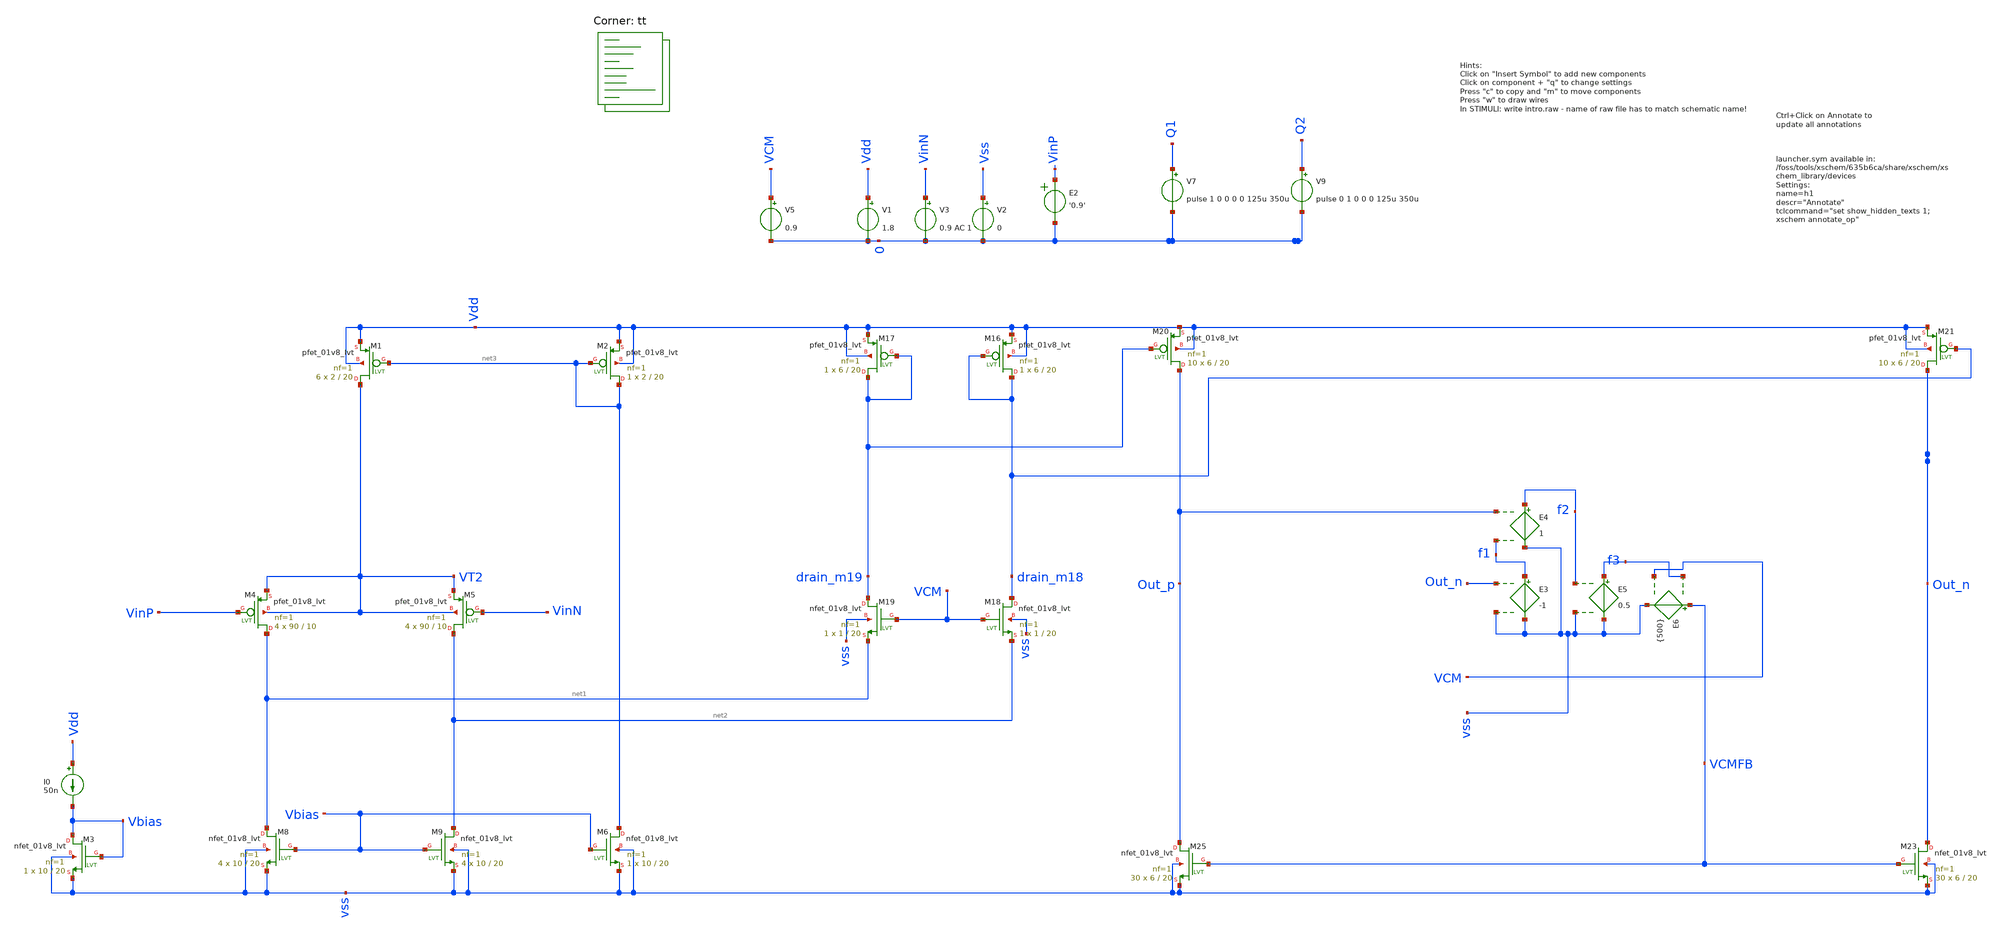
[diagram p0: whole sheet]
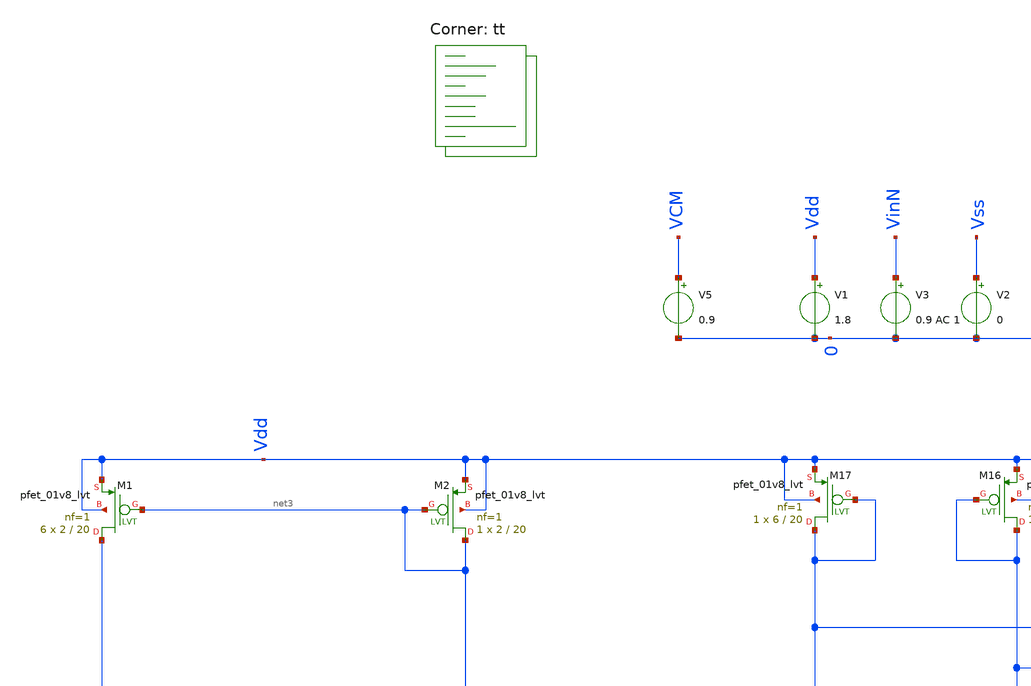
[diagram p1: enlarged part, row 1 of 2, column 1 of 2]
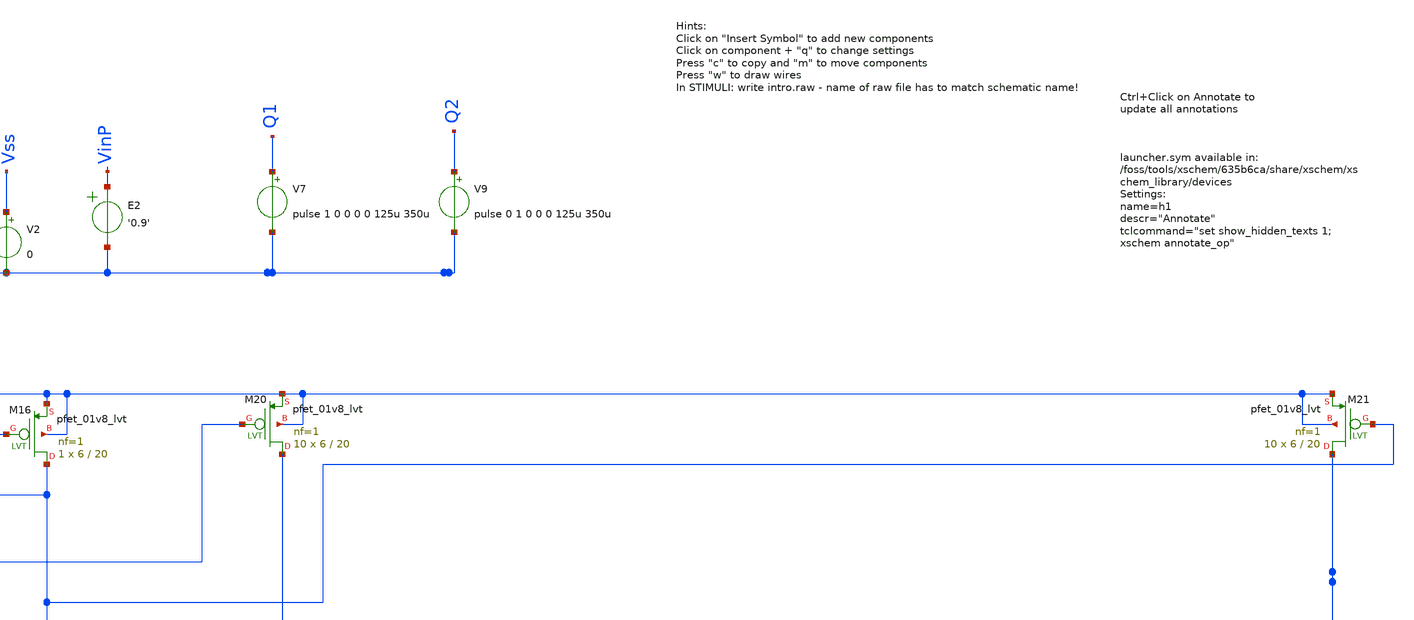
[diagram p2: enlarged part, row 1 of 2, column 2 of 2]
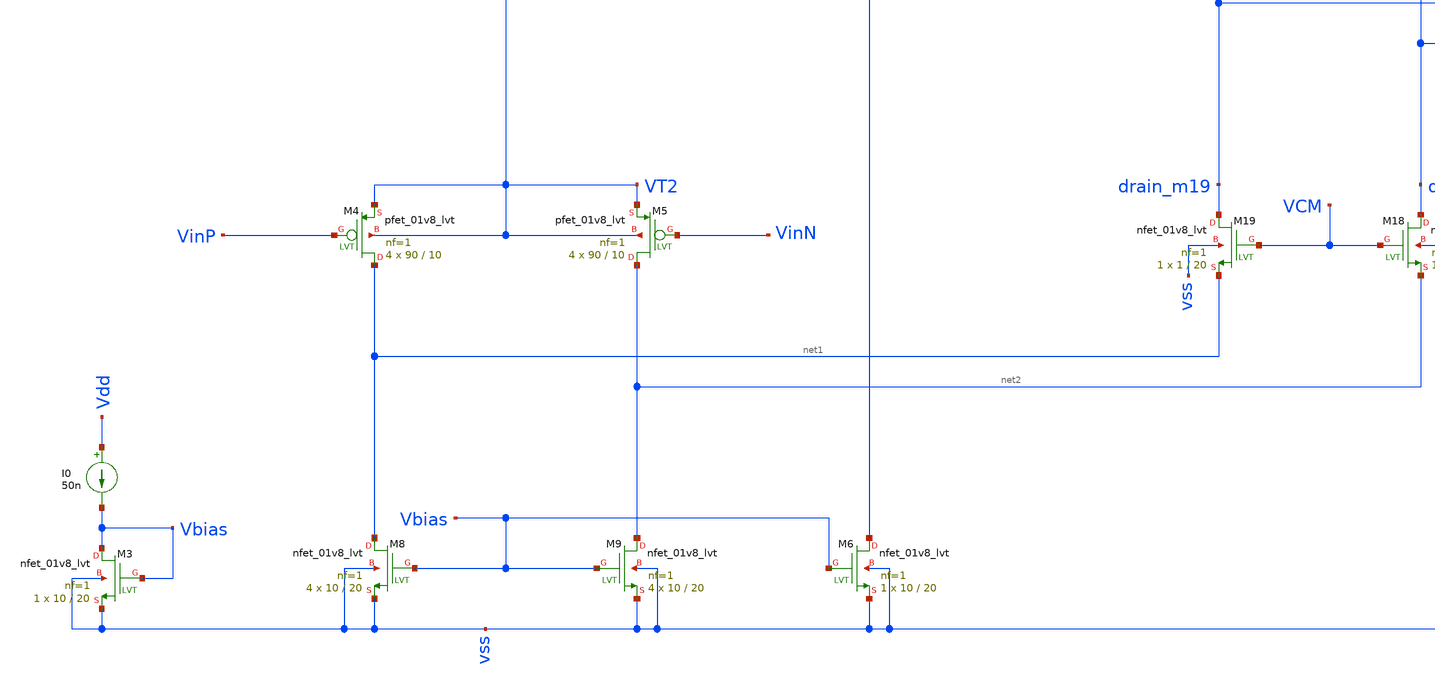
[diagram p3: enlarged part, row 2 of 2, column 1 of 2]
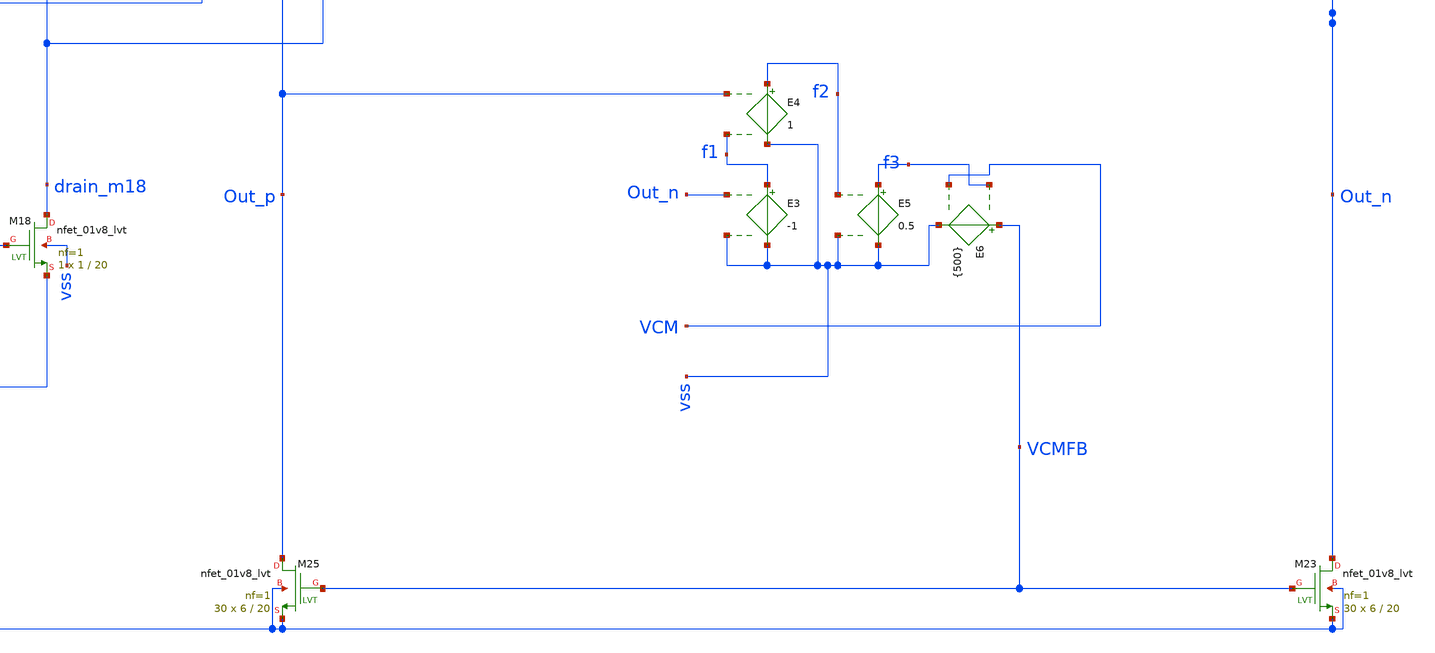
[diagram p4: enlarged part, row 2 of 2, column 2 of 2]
** sch_path: introlvt.sch
**.subckt introlvt
XM4 net1 VinP VT2 VT2 sky130_fd_pr__pfet_01v8_lvt L=10 W=90 nf=1 ad='int((nf+1)/2) * W/nf * 0.29' as='int((nf+2)/2) * W/nf * 0.29'
+ pd='2*int((nf+1)/2) * (W/nf + 0.29)' ps='2*int((nf+2)/2) * (W/nf + 0.29)' nrd='0.29 / W' nrs='0.29 / W'
+ sa=0 sb=0 sd=0 mult=4 m=4
XM5 net2 VinN VT2 VT2 sky130_fd_pr__pfet_01v8_lvt L=10 W=90 nf=1 ad='int((nf+1)/2) * W/nf * 0.29' as='int((nf+2)/2) * W/nf * 0.29'
+ pd='2*int((nf+1)/2) * (W/nf + 0.29)' ps='2*int((nf+2)/2) * (W/nf + 0.29)' nrd='0.29 / W' nrs='0.29 / W'
+ sa=0 sb=0 sd=0 mult=4 m=4
XM8 net1 Vbias vss vss sky130_fd_pr__nfet_01v8_lvt L=20 W=10 nf=1 ad='int((nf+1)/2) * W/nf * 0.29' as='int((nf+2)/2) * W/nf * 0.29'
+ pd='2*int((nf+1)/2) * (W/nf + 0.29)' ps='2*int((nf+2)/2) * (W/nf + 0.29)' nrd='0.29 / W' nrs='0.29 / W'
+ sa=0 sb=0 sd=0 mult=4 m=4
XM9 net2 Vbias vss vss sky130_fd_pr__nfet_01v8_lvt L=20 W=10 nf=1 ad='int((nf+1)/2) * W/nf * 0.29' as='int((nf+2)/2) * W/nf * 0.29'
+ pd='2*int((nf+1)/2) * (W/nf + 0.29)' ps='2*int((nf+2)/2) * (W/nf + 0.29)' nrd='0.29 / W' nrs='0.29 / W'
+ sa=0 sb=0 sd=0 mult=4 m=4
XM16 drain_m18 drain_m18 Vdd Vdd sky130_fd_pr__pfet_01v8_lvt L=20 W=6 nf=1 ad='int((nf+1)/2) * W/nf * 0.29'
+ as='int((nf+2)/2) * W/nf * 0.29' pd='2*int((nf+1)/2) * (W/nf + 0.29)' ps='2*int((nf+2)/2) * (W/nf + 0.29)'
+ nrd='0.29 / W' nrs='0.29 / W' sa=0 sb=0 sd=0 mult=1 m=1
XM17 drain_m19 drain_m19 Vdd Vdd sky130_fd_pr__pfet_01v8_lvt L=20 W=6 nf=1 ad='int((nf+1)/2) * W/nf * 0.29'
+ as='int((nf+2)/2) * W/nf * 0.29' pd='2*int((nf+1)/2) * (W/nf + 0.29)' ps='2*int((nf+2)/2) * (W/nf + 0.29)'
+ nrd='0.29 / W' nrs='0.29 / W' sa=0 sb=0 sd=0 mult=1 m=1
XM18 drain_m18 VCM net2 vss sky130_fd_pr__nfet_01v8_lvt L=20 W=1 nf=1 ad='int((nf+1)/2) * W/nf * 0.29'
+ as='int((nf+2)/2) * W/nf * 0.29' pd='2*int((nf+1)/2) * (W/nf + 0.29)' ps='2*int((nf+2)/2) * (W/nf + 0.29)'
+ nrd='0.29 / W' nrs='0.29 / W' sa=0 sb=0 sd=0 mult=1 m=1
XM19 drain_m19 VCM net1 vss sky130_fd_pr__nfet_01v8_lvt L=20 W=1 nf=1 ad='int((nf+1)/2) * W/nf * 0.29'
+ as='int((nf+2)/2) * W/nf * 0.29' pd='2*int((nf+1)/2) * (W/nf + 0.29)' ps='2*int((nf+2)/2) * (W/nf + 0.29)'
+ nrd='0.29 / W' nrs='0.29 / W' sa=0 sb=0 sd=0 mult=1 m=1
XM20 Out_p drain_m19 Vdd Vdd sky130_fd_pr__pfet_01v8_lvt L=20 W=6 nf=1 ad='int((nf+1)/2) * W/nf * 0.29'
+ as='int((nf+2)/2) * W/nf * 0.29' pd='2*int((nf+1)/2) * (W/nf + 0.29)' ps='2*int((nf+2)/2) * (W/nf + 0.29)'
+ nrd='0.29 / W' nrs='0.29 / W' sa=0 sb=0 sd=0 mult=10 m=10
XM21 Out_n drain_m18 Vdd Vdd sky130_fd_pr__pfet_01v8_lvt L=20 W=6 nf=1 ad='int((nf+1)/2) * W/nf * 0.29'
+ as='int((nf+2)/2) * W/nf * 0.29' pd='2*int((nf+1)/2) * (W/nf + 0.29)' ps='2*int((nf+2)/2) * (W/nf + 0.29)'
+ nrd='0.29 / W' nrs='0.29 / W' sa=0 sb=0 sd=0 mult=10 m=10
XM23 Out_n VCMFB vss vss sky130_fd_pr__nfet_01v8_lvt L=20 W=6 nf=1 ad='int((nf+1)/2) * W/nf * 0.29' as='int((nf+2)/2) * W/nf * 0.29'
+ pd='2*int((nf+1)/2) * (W/nf + 0.29)' ps='2*int((nf+2)/2) * (W/nf + 0.29)' nrd='0.29 / W' nrs='0.29 / W'
+ sa=0 sb=0 sd=0 mult=30 m=30
XM25 Out_p VCMFB vss vss sky130_fd_pr__nfet_01v8_lvt L=20 W=6 nf=1 ad='int((nf+1)/2) * W/nf * 0.29' as='int((nf+2)/2) * W/nf * 0.29'
+ pd='2*int((nf+1)/2) * (W/nf + 0.29)' ps='2*int((nf+2)/2) * (W/nf + 0.29)' nrd='0.29 / W' nrs='0.29 / W'
+ sa=0 sb=0 sd=0 mult=30 m=30
E2 VinP 0 VOL=' '0.9' '
V1 Vdd 0 1.8
V2 Vss 0 0
V5 VCM 0 0.9
V9 Q2 0 pulse 0 1 0 0 0 125u 350u
V7 Q1 0 pulse 1 0 0 0 0 125u 350u
XM1 VT2 net3 Vdd Vdd sky130_fd_pr__pfet_01v8_lvt L=20 W=2 nf=1 ad='int((nf+1)/2) * W/nf * 0.29' as='int((nf+2)/2) * W/nf * 0.29'
+ pd='2*int((nf+1)/2) * (W/nf + 0.29)' ps='2*int((nf+2)/2) * (W/nf + 0.29)' nrd='0.29 / W' nrs='0.29 / W'
+ sa=0 sb=0 sd=0 mult=6 m=6
XM2 net3 net3 Vdd Vdd sky130_fd_pr__pfet_01v8_lvt L=20 W=2 nf=1 ad='int((nf+1)/2) * W/nf * 0.29' as='int((nf+2)/2) * W/nf * 0.29'
+ pd='2*int((nf+1)/2) * (W/nf + 0.29)' ps='2*int((nf+2)/2) * (W/nf + 0.29)' nrd='0.29 / W' nrs='0.29 / W'
+ sa=0 sb=0 sd=0 mult=1 m=1
V3 VinN 0 0.9 AC 1
I0 Vdd Vbias 50n
XM3 Vbias Vbias vss vss sky130_fd_pr__nfet_01v8_lvt L=20 W=10 nf=1 ad='int((nf+1)/2) * W/nf * 0.29' as='int((nf+2)/2) * W/nf * 0.29'
+ pd='2*int((nf+1)/2) * (W/nf + 0.29)' ps='2*int((nf+2)/2) * (W/nf + 0.29)' nrd='0.29 / W' nrs='0.29 / W'
+ sa=0 sb=0 sd=0 mult=1 m=1
XM6 net3 Vbias vss vss sky130_fd_pr__nfet_01v8_lvt L=20 W=10 nf=1 ad='int((nf+1)/2) * W/nf * 0.29' as='int((nf+2)/2) * W/nf * 0.29'
+ pd='2*int((nf+1)/2) * (W/nf + 0.29)' ps='2*int((nf+2)/2) * (W/nf + 0.29)' nrd='0.29 / W' nrs='0.29 / W'
+ sa=0 sb=0 sd=0 mult=1 m=1
E3 f1 vss Out_n vss -1
E4 f2 vss Out_p f1 1
E5 f3 vss f2 vss 0.5
E6 VCMFB vss f3 VCM {500}
**** begin user architecture code
.lib $::SKYWATER_MODELS/sky130.lib.spice tt


.options savecurrents
*ic v(VM5)=0.9 v(VM6)=0.9
.control


save all

save @m.xm11.msky130_fd_pr__pfet_01v8_lvt[id]
save @m.xm11.msky130_fd_pr__pfet_01v8_lvt[vgs]


*nmos
save @m.xm3.msky130_fd_pr__nfet_01v8_lvt[vgs]
save @m.xm3.msky130_fd_pr__nfet_01v8_lvt[vth]
save @m.xm3.msky130_fd_pr__nfet_01v8_lvt[vds]

save @m.xm6.msky130_fd_pr__nfet_01v8_lvt[vgs]
save @m.xm6.msky130_fd_pr__nfet_01v8_lvt[vth]
save @m.xm6.msky130_fd_pr__nfet_01v8_lvt[vds]

save @m.xm8.msky130_fd_pr__nfet_01v8_lvt[vgs]
save @m.xm8.msky130_fd_pr__nfet_01v8_lvt[vth]
save @m.xm8.msky130_fd_pr__nfet_01v8_lvt[vds]

save @m.xm9.msky130_fd_pr__nfet_01v8_lvt[vgs]
save @m.xm9.msky130_fd_pr__nfet_01v8_lvt[vth]
save @m.xm9.msky130_fd_pr__nfet_01v8_lvt[vds]

save @m.xm18.msky130_fd_pr__nfet_01v8_lvt[vgs]
save @m.xm18.msky130_fd_pr__nfet_01v8_lvt[vth]
save @m.xm18.msky130_fd_pr__nfet_01v8_lvt[vds]

save @m.xm19.msky130_fd_pr__nfet_01v8_lvt[vgs]
save @m.xm19.msky130_fd_pr__nfet_01v8_lvt[vth]
save @m.xm19.msky130_fd_pr__nfet_01v8_lvt[vds]

save @m.xm25.msky130_fd_pr__nfet_01v8_lvt[vgs]
save @m.xm25.msky130_fd_pr__nfet_01v8_lvt[vth]
save @m.xm25.msky130_fd_pr__nfet_01v8_lvt[vds]

*pmos

save @m.xm1.msky130_fd_pr__pfet_01v8_lvt[vgs]
save @m.xm1.msky130_fd_pr__pfet_01v8_lvt[vth]
save @m.xm1.msky130_fd_pr__pfet_01v8_lvt[vds]


save @m.xm2.msky130_fd_pr__pfet_01v8_lvt[vgs]
save @m.xm2.msky130_fd_pr__pfet_01v8_lvt[vth]
save @m.xm2.msky130_fd_pr__pfet_01v8_lvt[vds]


save @m.xm10.msky130_fd_pr__pfet_01v8_lvt[vgs]
save @m.xm10.msky130_fd_pr__pfet_01v8_lvt[vth]
save @m.xm10.msky130_fd_pr__pfet_01v8_lvt[vds]

save @m.xm13.msky130_fd_pr__pfet_01v8_lvt[vgs]
save @m.xm13.msky130_fd_pr__pfet_01v8_lvt[vth]
save @m.xm13.msky130_fd_pr__pfet_01v8_lvt[vds]

save @m.xm4.msky130_fd_pr__pfet_01v8_lvt[vgs]
save @m.xm4.msky130_fd_pr__pfet_01v8_lvt[vth]
save @m.xm4.msky130_fd_pr__pfet_01v8_lvt[vds]

save @m.xm5.msky130_fd_pr__pfet_01v8_lvt[vgs]
save @m.xm5.msky130_fd_pr__pfet_01v8_lvt[vth]
save @m.xm5.msky130_fd_pr__pfet_01v8_lvt[vds]

save @m.xm16.msky130_fd_pr__pfet_01v8_lvt[vgs]
save @m.xm16.msky130_fd_pr__pfet_01v8_lvt[vth]
save @m.xm16.msky130_fd_pr__pfet_01v8_lvt[vds]

save @m.xm17.msky130_fd_pr__pfet_01v8_lvt[vgs]
save @m.xm17.msky130_fd_pr__pfet_01v8_lvt[vth]
save @m.xm17.msky130_fd_pr__pfet_01v8_lvt[vds]

save @m.xm3.msky130_fd_pr__pfet_01v8_lvt[vgs]
save @m.xm3.msky130_fd_pr__pfet_01v8_lvt[vth]
save @m.xm3.msky130_fd_pr__pfet_01v8_lvt[vds]

save @m.xm20.msky130_fd_pr__pfet_01v8_lvt[vgs]
save @m.xm20.msky130_fd_pr__pfet_01v8_lvt[vth]
save @m.xm20.msky130_fd_pr__pfet_01v8_lvt[vds]

save @m.xm2.msky130_fd_pr__pfet_01v8_lvt[vgs]
save @m.xm2.msky130_fd_pr__pfet_01v8_lvt[vth]
save @m.xm2.msky130_fd_pr__pfet_01v8_lvt[vds]

save @m.xm21.msky130_fd_pr__pfet_01v8_lvt[vgs]
save @m.xm21.msky130_fd_pr__pfet_01v8_lvt[vth]
save @m.xm21.msky130_fd_pr__pfet_01v8_lvt[vds]

save @m.xm7.msky130_fd_pr__nfet_01v8_lvt[vth]

save @m.xm1.msky130_fd_pr__pfet_01v8[vgs]

save @m.xm1.msky130_fd_pr__nfet_01v8_lvt[gm]


save @m.xm1.msky130_fd_pr__nfet_01v8_lvt[gds]
save @m.xm2.msky130_fd_pr__pfet_01v8_lvt[gm]

save @m.xm23.msky130_fd_pr__nfet_01v8[cgs]
save @m.xm4.msky130_fd_pr__pfet_01v8[cgs]
save @m.xm2.msky130_fd_pr__pfet_01v8_lvt[cgs]



save @m.xm2.msky130_fd_pr__pfet_01v8_lvt[gds]


op
*remzerovec
write introlvt.raw
*set appendwrite

*dc V1 0 1.8 0.01
*plot @m.xm1.msky130_fd_pr__nfet_01v8_lvt[id] @m.xm2.msky130_fd_pr__pfet_01v8_lvt[id]
*remzerovec
*write intro.raw

.endc
.control
let vth=@M.XM25.msky130_fd_pr__nfet_01v8_lvt[vgs]


noise V(Out_p,Out_n) V3 dec 100 0.1 128
print inoise_total onoise_total
setplot noise1
plot inoise_spectrum




tran 1n 1u
save all
plot v(Out_p)
plot v(Out_p)-v(Out_n)
plot v(@m.xm25.msky130_fd_pr__nfet_01v8_lvt[vth]) v(@m.xm25.msky130_fd_pr__nfet_01v8_lvt[vgs])
plot
+ v(@m.xm25.msky130_fd_pr__nfet_01v8_lvt[vds])-v(@m.xm25.msky130_fd_pr__nfet_01v8_lvt[vgs])+v(@m.xm25.msky130_fd_pr__nfet_01v8_lvt[vth])

.endc






.include $::SKYWATER_STDCELLS/sky130_fd_sc_hd.spice

**** end user architecture code
**.ends
.end
